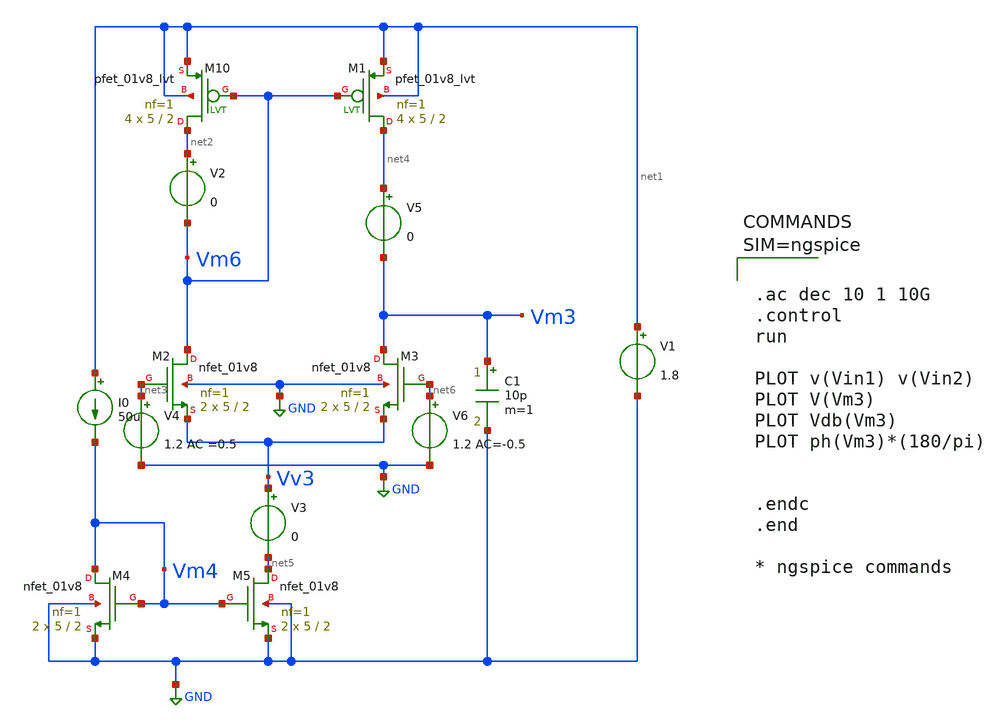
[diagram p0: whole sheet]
** sch_path: spice/diff_amp_ac.sch
**.subckt diff_amp_ac
XM10 net2 Vm6 net1 net1 sky130_fd_pr__pfet_01v8_lvt L=2 W=5 nf=1 ad='int((1 + 1)/2) * 5 / 1 * 0.29' as='int((1 + 2)/2) * 5 / 1 * 0.29'
+ pd='2*int((1 + 1)/2) * (5 / 1 + 0.29)' ps='2*int((1 + 2)/2) * (5 / 1 + 0.29)' nrd='0.29 / 5 ' nrs='0.29 / 5 '
+ sa=0 sb=0 sd=0 mult=4 m=4
XM1 net4 Vm6 net1 net1 sky130_fd_pr__pfet_01v8_lvt L=2 W=5 nf=1 ad='int((1 + 1)/2) * 5 / 1 * 0.29' as='int((1 + 2)/2) * 5 / 1 * 0.29'
+ pd='2*int((1 + 1)/2) * (5 / 1 + 0.29)' ps='2*int((1 + 2)/2) * (5 / 1 + 0.29)' nrd='0.29 / 5 ' nrs='0.29 / 5 '
+ sa=0 sb=0 sd=0 mult=4 m=4
XM3 Vm3 net6 Vv3 GND sky130_fd_pr__nfet_01v8 L=2 W=5 nf=1 ad='int((1 + 1)/2) * 5 / 1 * 0.29' as='int((1 + 2)/2) * 5 / 1 * 0.29'
+ pd='2*int((1 + 1)/2) * (5 / 1 + 0.29)' ps='2*int((1 + 2)/2) * (5 / 1 + 0.29)' nrd='0.29 / 5 ' nrs='0.29 / 5 '
+ sa=0 sb=0 sd=0 mult=2 m=2
XM4 Vm4 Vm4 GND GND sky130_fd_pr__nfet_01v8 L=2 W=5 nf=1 ad='int((1 + 1)/2) * 5 / 1 * 0.29' as='int((1 + 2)/2) * 5 / 1 * 0.29'
+ pd='2*int((1 + 1)/2) * (5 / 1 + 0.29)' ps='2*int((1 + 2)/2) * (5 / 1 + 0.29)' nrd='0.29 / 5 ' nrs='0.29 / 5 '
+ sa=0 sb=0 sd=0 mult=2 m=2
XM5 net5 Vm4 GND GND sky130_fd_pr__nfet_01v8 L=2 W=5 nf=1 ad='int((1 + 1)/2) * 5 / 1 * 0.29' as='int((1 + 2)/2) * 5 / 1 * 0.29'
+ pd='2*int((1 + 1)/2) * (5 / 1 + 0.29)' ps='2*int((1 + 2)/2) * (5 / 1 + 0.29)' nrd='0.29 / 5 ' nrs='0.29 / 5 '
+ sa=0 sb=0 sd=0 mult=2 m=2
I0 net1 Vm4 50u
C1 Vm3 GND 10p m=1
V2 net2 Vm6 0
V1 net1 GND 1.8
V3 Vv3 net5 0
V4 net3 GND 1.2 AC =0.5
XM2 Vm6 net3 Vv3 GND sky130_fd_pr__nfet_01v8 L=2 W=5 nf=1 ad='int((1 + 1)/2) * 5 / 1 * 0.29' as='int((1 + 2)/2) * 5 / 1 * 0.29'
+ pd='2*int((1 + 1)/2) * (5 / 1 + 0.29)' ps='2*int((1 + 2)/2) * (5 / 1 + 0.29)' nrd='0.29 / 5 ' nrs='0.29 / 5 '
+ sa=0 sb=0 sd=0 mult=2 m=2
V5 net4 Vm3 0
V6 net6 GND 1.2 AC=-0.5
**** begin user architecture code

** opencircuitdesign pdks install
.lib $::SKYWATER_MODELS/sky130.lib.spice tt




.ac dec 10 1 10G
.control
run

PLOT v(Vin1) v(Vin2)
PLOT V(Vm3)
PLOT Vdb(Vm3)
PLOT ph(Vm3)*(180/pi)


.endc
.end

* ngspice commands



**** end user architecture code
**.ends
.GLOBAL GND
.end
